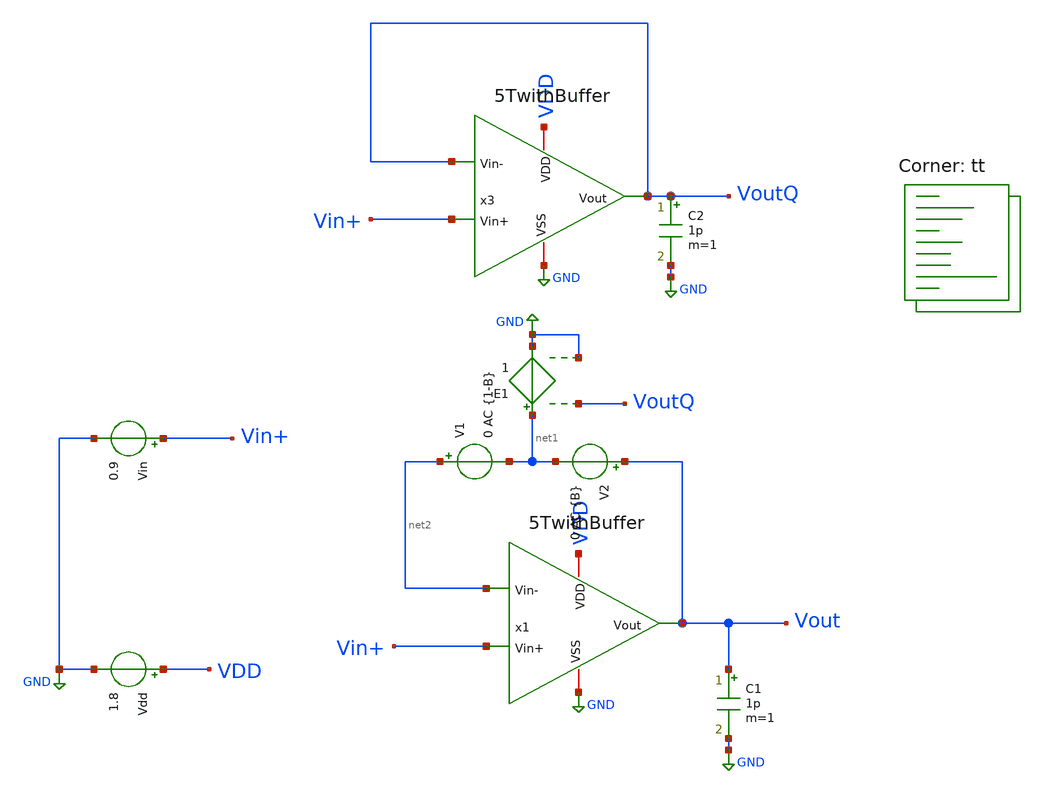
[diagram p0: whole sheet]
** sch_path: xschem/test/xschem/5T_op_loop.sch
**.subckt 5T_op_loop
Vdd VDD GND 1.8
.save i(vdd)
Vin Vin+ GND 0.9
C1 Vout GND 1p m=1
V2 Vout net1 0 AC {B}
.save i(v2)
V1 net2 net1 0 AC {1-B}
.save i(v1)
C2 VoutQ GND 1p m=1
E1 net1 GND VoutQ GND 1
x3 VDD VoutQ VoutQ Vin+ GND 5TwithBuffer
x1 VDD Vout net2 Vin+ GND 5TwithBuffer
**** begin user architecture code
.lib $::SKYWATER_MODELS/sky130.lib.spice tt


.param B=0
.savecurrents
.control

save @m.x1.xm5.msky130_fd_pr__pfet_01v8_lvt[gm]
save @m.x1.xm5.msky130_fd_pr__pfet_01v8_lvt[gds]
save @m.x1.xm5.msky130_fd_pr__pfet_01v8_lvt[id]
save @m.x1.xm5.msky130_fd_pr__pfet_01v8_lvt[vgs] -  @m.x1.xm5.msky130_fd_pr__pfet_01v8_lvt[vth]
save @m.x1.xm5.msky130_fd_pr__pfet_01v8_lvt[vds]



save @m.x1.xm1.msky130_fd_pr__nfet_01v8[gm]
save @m.x1.xm1.msky130_fd_pr__nfet_01v8[gds]
save @m.x1.xm1.msky130_fd_pr__nfet_01v8[id]
save @m.x1.xm1.msky130_fd_pr__nfet_01v8[vgs]
save @m.x1.xm1.msky130_fd_pr__nfet_01v8[vds]

save @m.x1.xm3.msky130_fd_pr__nfet_01v8[gm]
save @m.x1.xm3.msky130_fd_pr__nfet_01v8[gds]
save @m.x1.xm3.msky130_fd_pr__nfet_01v8[id]
save @m.x1.xm3.msky130_fd_pr__nfet_01v8[vgs]
save @m.x1.xm3.msky130_fd_pr__nfet_01v8[vds]



save @m.x1.xm7.msky130_fd_pr__pfet_01v8_lvt[gm]
save @m.x1.xm7.msky130_fd_pr__pfet_01v8_lvt[gds]
save @m.x1.xm7.msky130_fd_pr__pfet_01v8_lvt[id]
save @m.x1.xm7.msky130_fd_pr__pfet_01v8_lvt[vgs]
save @m.x1.xm7.msky130_fd_pr__pfet_01v8_lvt[vds]









save @m.x1.xm9.msky130_fd_pr__pfet_01v8_lvt[gm]
save @m.x1.xm9.msky130_fd_pr__pfet_01v8_lvt[gds]
save @m.x1.xm9.msky130_fd_pr__pfet_01v8_lvt[id]
save @m.x1.xm9.msky130_fd_pr__pfet_01v8_lvt[vgs]
save @m.x1.xm9.msky130_fd_pr__pfet_01v8_lvt[vds]

save @m.x1.xm11.msky130_fd_pr__pfet_01v8_lvt[gm]
save @m.x1.xm11.msky130_fd_pr__pfet_01v8_lvt[gds]
save @m.x1.xm11.msky130_fd_pr__pfet_01v8_lvt[id]
save @m.x1.xm11.msky130_fd_pr__pfet_01v8_lvt[vgs]
save @m.x1.xm11.msky130_fd_pr__pfet_01v8_lvt[vds]




save v(Vout)

 op
 ac dec 20 1 1e12
 alterparam B=1
 reset
 ac dec 20 1 1e12
 meas ac freq_at_gain db(v(Vout))=0
 meas ac phase_at_gc ph(v(Vout)) at freq_at_gain

 setplot new
 set curplottitle=Loopgain
 let frequency = ac1.frequency

 let T = (ac1.i(V2)+ac2.i(V1))/(ac1.i(V1)+ac2.i(V2))
 let Tmag = db(T)
 let Tphase = 180 * cph(T)/pi
 let Pm = 180 + Tphase
 plot Tmag Tphase Pm xlog
 plot Tmag xlog

 plot Tphase xlog

 print @m.x1.xm5.msky130_fd_pr__pfet_01v8_lvt[gm]
 print @m.x1.xm5.msky130_fd_pr__pfet_01v8_lvt[gds]
 print @m.x1.xm5.msky130_fd_pr__pfet_01v8_lvt[id]
 print @m.x1.xm5.msky130_fd_pr__pfet_01v8_lvt[vgs]
 print @m.x1.xm5.msky130_fd_pr__pfet_01v8_lvt[vds]

print @m.x1.xm5.msky130_fd_pr__pfet_01v8_lvt[vgs] -  @m.x1.xm5.msky130_fd_pr__pfet_01v8_lvt[vth]

print @m.x1.xm1.msky130_fd_pr__pfet_01v8_lvt[vgs] -  @m.x1.xm1.msky130_fd_pr__pfet_01v8_lvt[vth]

 print @m.x1.xm7.msky130_fd_pr__pfet_01v8_lvt[gm]
 print @m.x1.xm7.msky130_fd_pr__pfet_01v8_lvt[gds]
 print @m.x1.xm7.msky130_fd_pr__pfet_01v8_lvt[id]
 print @m.x1.xm7.msky130_fd_pr__pfet_01v8_lvt[vgs]
 print @m.x1.xm7.msky130_fd_pr__pfet_01v8_lvt[vds]

 print @m.x1.xm9.msky130_fd_pr__pfet_01v8_lvt[gm]
 print @m.x1.xm9.msky130_fd_pr__pfet_01v8_lvt[gds]
 print @m.x1.xm9.msky130_fd_pr__pfet_01v8_lvt[id]
 print @m.x1.xm9.msky130_fd_pr__pfet_01v8_lvt[vgs]
 print @m.x1.xm9.msky130_fd_pr__pfet_01v8_lvt[vds]

 print @m.x1.xm11.msky130_fd_pr__pfet_01v8_lvt[gm]
 print @m.x1.xm11.msky130_fd_pr__pfet_01v8_lvt[gds]
 print @m.x1.xm11.msky130_fd_pr__pfet_01v8_lvt[id]
 print @m.x1.xm11.msky130_fd_pr__pfet_01v8_lvt[vgs]
 print @m.x1.xm11.msky130_fd_pr__pfet_01v8_lvt[vds]

 print @m.x1.xm10.msky130_fd_pr__pfet_01v8_lvt[gm]
 print @m.x1.xm10.msky130_fd_pr__pfet_01v8_lvt[gds]
 print @m.x1.xm10.msky130_fd_pr__pfet_01v8_lvt[id]
 print @m.x1.xm10.msky130_fd_pr__pfet_01v8_lvt[vgs]
 print @m.x1.xm10.msky130_fd_pr__pfet_01v8_lvt[vds]



 print @m.x1.xm1.msky130_fd_pr__nfet_01v8[gm]
 print @m.x1.xm1.msky130_fd_pr__nfet_01v8[gds]
 print @m.x1.xm1.msky130_fd_pr__nfet_01v8[id]
 print @m.x1.xm1.msky130_fd_pr__nfet_01v8[vgs] - @m.x1.xm1.msky130_fd_pr__nfet_01v8[vth]
 print @m.x1.xm1.msky130_fd_pr__nfet_01v8[vds]

 print @m.x1.xm3.msky130_fd_pr__nfet_01v8[gm]
 print @m.x1.xm3.msky130_fd_pr__nfet_01v8[gds]
 print @m.x1.xm3.msky130_fd_pr__nfet_01v8[id]
 print @m.x1.xm3.msky130_fd_pr__nfet_01v8[vgs]
 print @m.x1.xm3.msky130_fd_pr__nfet_01v8[vds]




 write OpenLoopTB.raw


.endc


**** end user architecture code
**.ends

* expanding   symbol:  amplifiers/dec24/5TwithBuffer.sym # of pins=5
** sym_path: amplifiers/dec24/5TwithBuffer.sym
** sch_path: amplifiers/dec24/5TwithBuffer.sch
.subckt 5TwithBuffer VDD Vout Vin- Vin+ VSS
*.iopin VDD
*.iopin VSS
*.ipin Vin-
*.ipin Vin+
*.opin Vout
I0 VDD Vb1 100u
XM1 net1 Vin+ Vsink VSS sky130_fd_pr__nfet_01v8 L=1 W=4 nf=1 ad='int((nf+1)/2) * W/nf * 0.29' as='int((nf+2)/2) * W/nf * 0.29'
+ pd='2*int((nf+1)/2) * (W/nf + 0.29)' ps='2*int((nf+2)/2) * (W/nf + 0.29)' nrd='0.29 / W' nrs='0.29 / W'
+ sa=0 sb=0 sd=0 mult=1 m=1
XM2 Vout Vin- Vsink VSS sky130_fd_pr__nfet_01v8 L=1 W=4 nf=1 ad='int((nf+1)/2) * W/nf * 0.29' as='int((nf+2)/2) * W/nf * 0.29'
+ pd='2*int((nf+1)/2) * (W/nf + 0.29)' ps='2*int((nf+2)/2) * (W/nf + 0.29)' nrd='0.29 / W' nrs='0.29 / W'
+ sa=0 sb=0 sd=0 mult=1 m=1
XM3 Vb1 Vb1 VSS VSS sky130_fd_pr__nfet_01v8 L=1 W=5 nf=1 ad='int((nf+1)/2) * W/nf * 0.29' as='int((nf+2)/2) * W/nf * 0.29'
+ pd='2*int((nf+1)/2) * (W/nf + 0.29)' ps='2*int((nf+2)/2) * (W/nf + 0.29)' nrd='0.29 / W' nrs='0.29 / W'
+ sa=0 sb=0 sd=0 mult=1 m=1
XM4 Vsink Vb1 VSS VSS sky130_fd_pr__nfet_01v8 L=1 W=5 nf=1 ad='int((nf+1)/2) * W/nf * 0.29' as='int((nf+2)/2) * W/nf * 0.29'
+ pd='2*int((nf+1)/2) * (W/nf + 0.29)' ps='2*int((nf+2)/2) * (W/nf + 0.29)' nrd='0.29 / W' nrs='0.29 / W'
+ sa=0 sb=0 sd=0 mult=1 m=1
XM7 VDD Vout net2 VSS sky130_fd_pr__nfet_01v8 L=1 W=20 nf=1 ad='int((nf+1)/2) * W/nf * 0.29' as='int((nf+2)/2) * W/nf * 0.29'
+ pd='2*int((nf+1)/2) * (W/nf + 0.29)' ps='2*int((nf+2)/2) * (W/nf + 0.29)' nrd='0.29 / W' nrs='0.29 / W'
+ sa=0 sb=0 sd=0 mult=1 m=1
XM8 net2 Vb1 VSS VSS sky130_fd_pr__nfet_01v8 L=1 W=5 nf=1 ad='int((nf+1)/2) * W/nf * 0.29' as='int((nf+2)/2) * W/nf * 0.29'
+ pd='2*int((nf+1)/2) * (W/nf + 0.29)' ps='2*int((nf+2)/2) * (W/nf + 0.29)' nrd='0.29 / W' nrs='0.29 / W'
+ sa=0 sb=0 sd=0 mult=5 m=5
XM5 net1 net1 VDD VDD sky130_fd_pr__pfet_01v8_lvt L=1 W=10 nf=1 ad='int((nf+1)/2) * W/nf * 0.29' as='int((nf+2)/2) * W/nf * 0.29'
+ pd='2*int((nf+1)/2) * (W/nf + 0.29)' ps='2*int((nf+2)/2) * (W/nf + 0.29)' nrd='0.29 / W' nrs='0.29 / W'
+ sa=0 sb=0 sd=0 mult=1 m=1
XM6 VDD net1 Vout VDD sky130_fd_pr__pfet_01v8_lvt L=1 W=10 nf=1 ad='int((nf+1)/2) * W/nf * 0.29' as='int((nf+2)/2) * W/nf * 0.29'
+ pd='2*int((nf+1)/2) * (W/nf + 0.29)' ps='2*int((nf+2)/2) * (W/nf + 0.29)' nrd='0.29 / W' nrs='0.29 / W'
+ sa=0 sb=0 sd=0 mult=1 m=1
.ends

.GLOBAL GND
.GLOBAL VDD
.end
